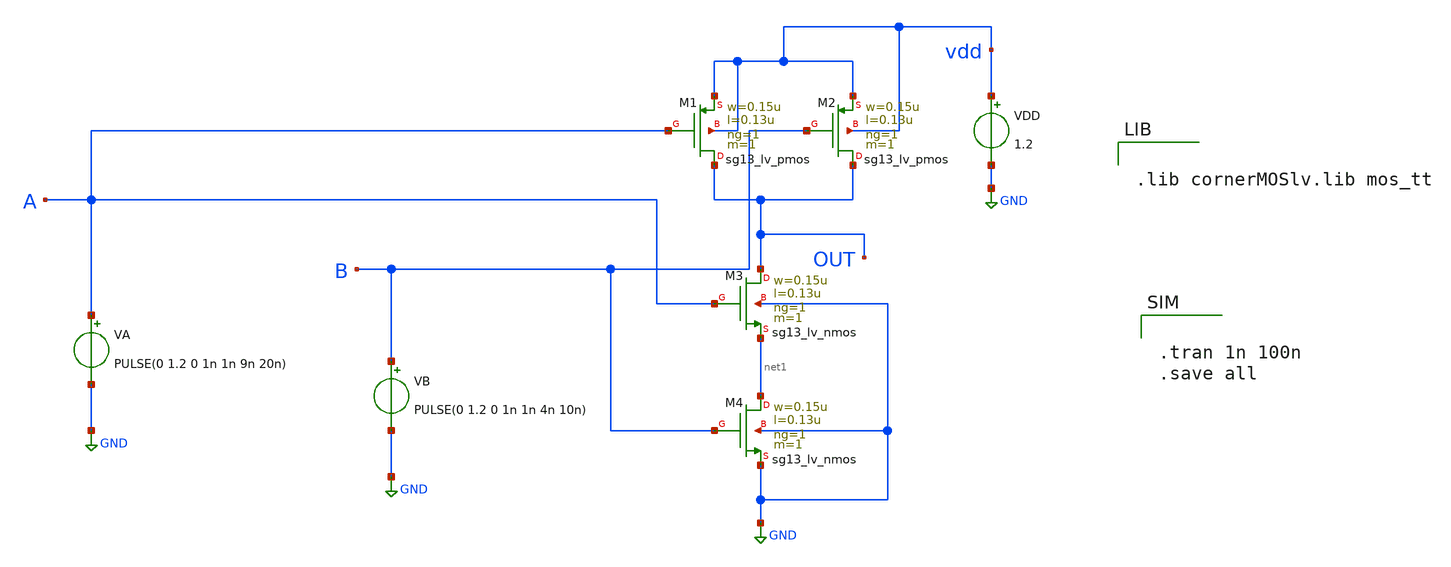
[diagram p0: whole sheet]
** sch_path: nand2.sch
**.subckt nand2
XM1 OUT A vdd vdd sg13_lv_pmos w=0.15u l=0.13u ng=1 m=1 mm_ok=1
XM2 OUT B vdd vdd sg13_lv_pmos w=0.15u l=0.13u ng=1 m=1 mm_ok=1
XM3 OUT A net1 GND sg13_lv_nmos w=0.15u l=0.13u ng=1 m=1 mm_ok=1
XM4 net1 B GND GND sg13_lv_nmos w=0.15u l=0.13u ng=1 m=1 mm_ok=1
VDD vdd GND 1.2
VA A GND PULSE(0 1.2 0 1n 1n 9n 20n)
VB B GND PULSE(0 1.2 0 1n 1n 4n 10n)
**** begin user architecture code


.lib cornerMOSlv.lib mos_tt



.tran 1n 100n
.save all


**** end user architecture code
**.ends
.GLOBAL GND
.end
